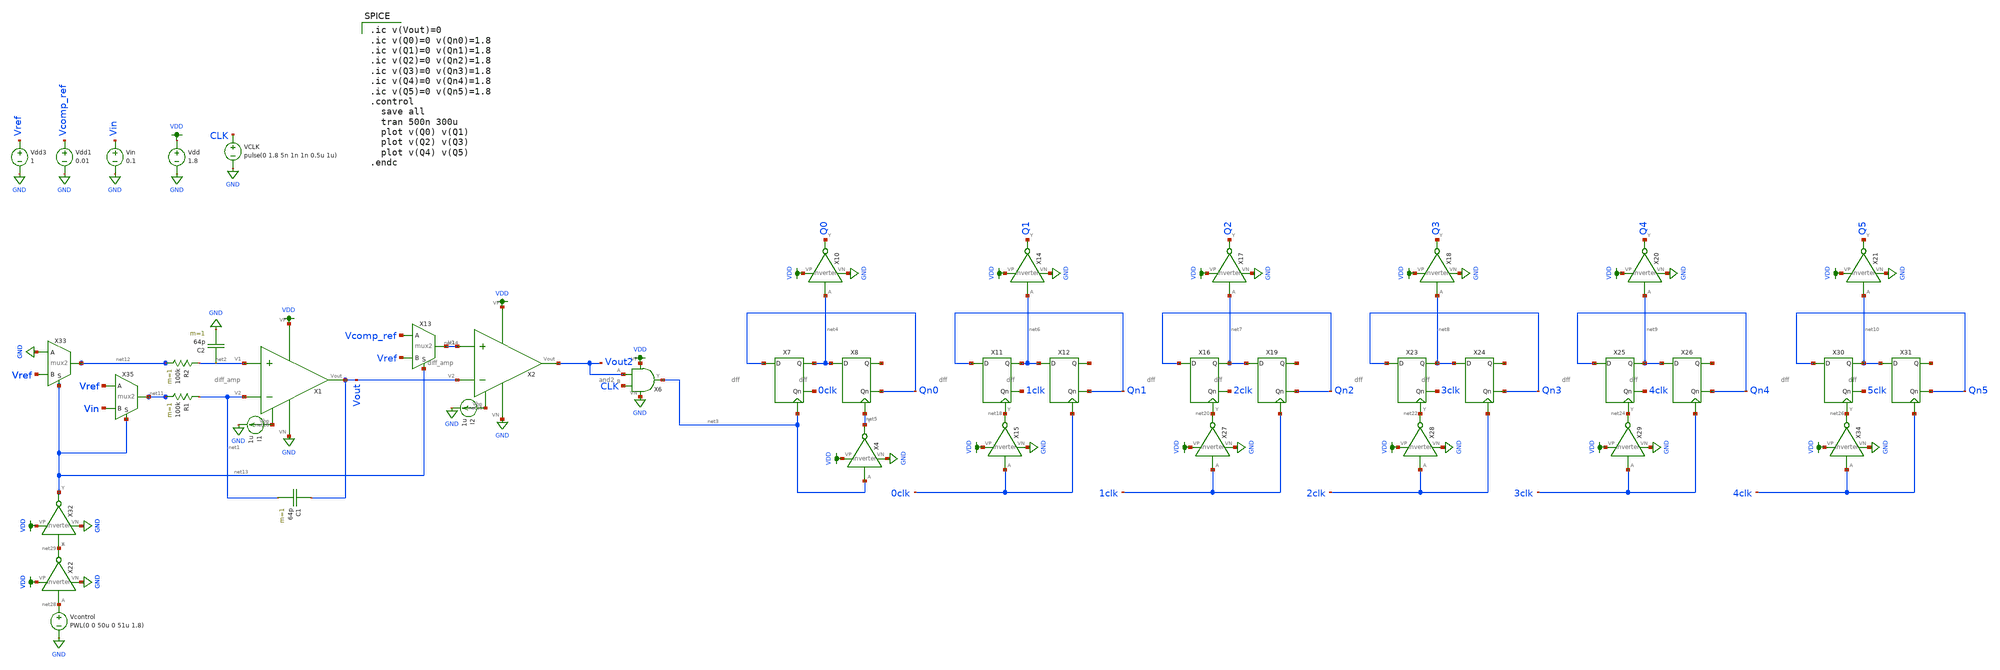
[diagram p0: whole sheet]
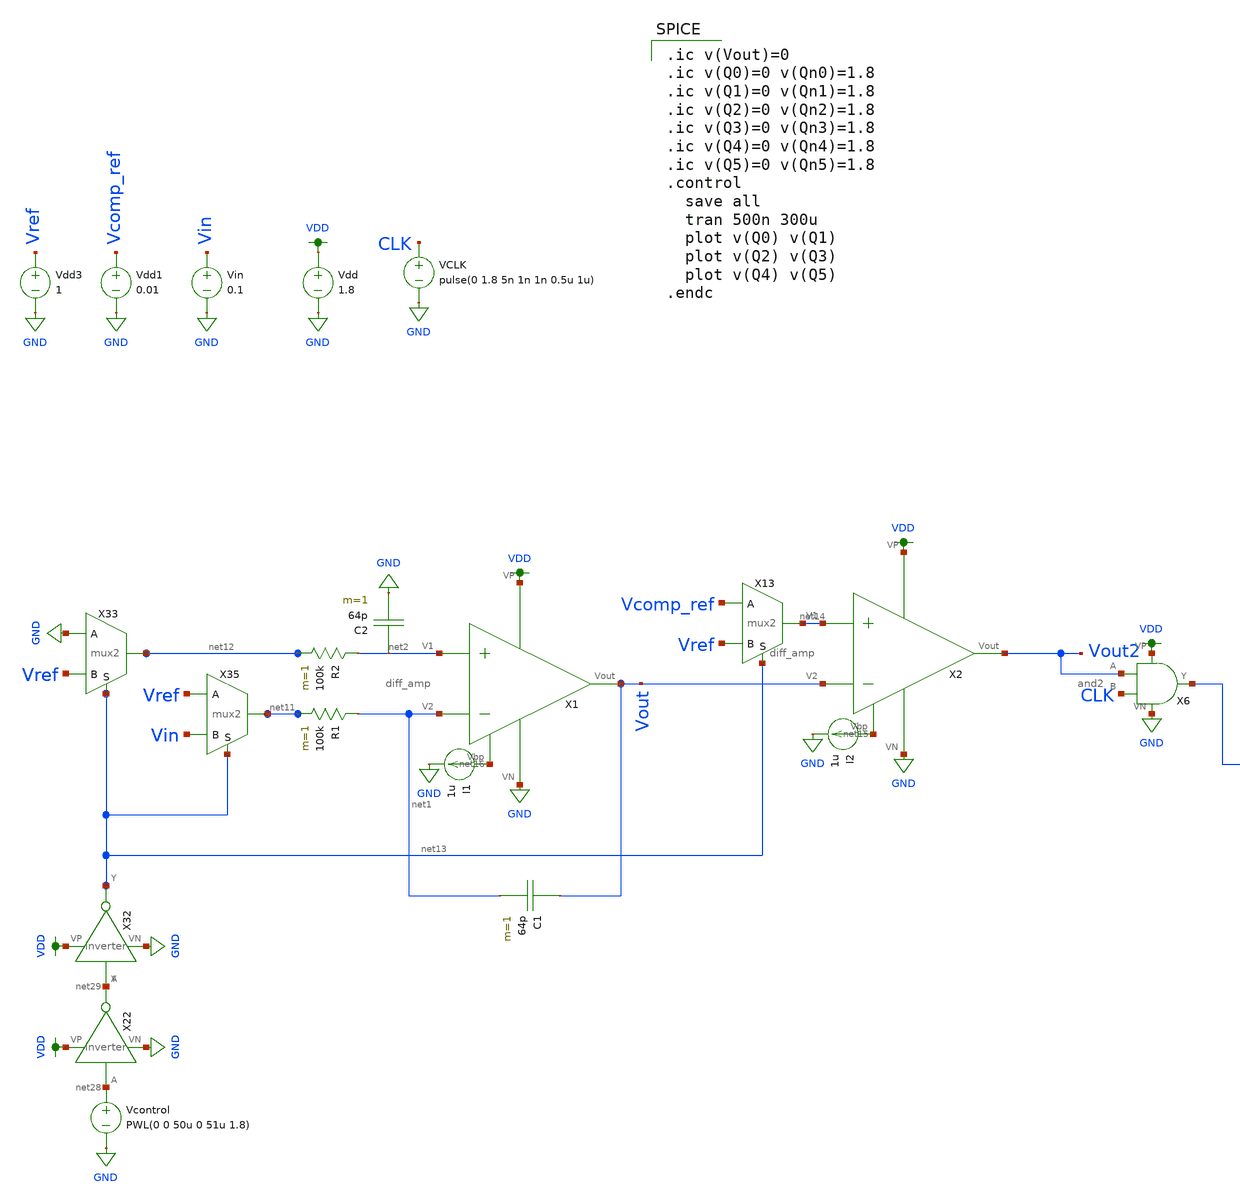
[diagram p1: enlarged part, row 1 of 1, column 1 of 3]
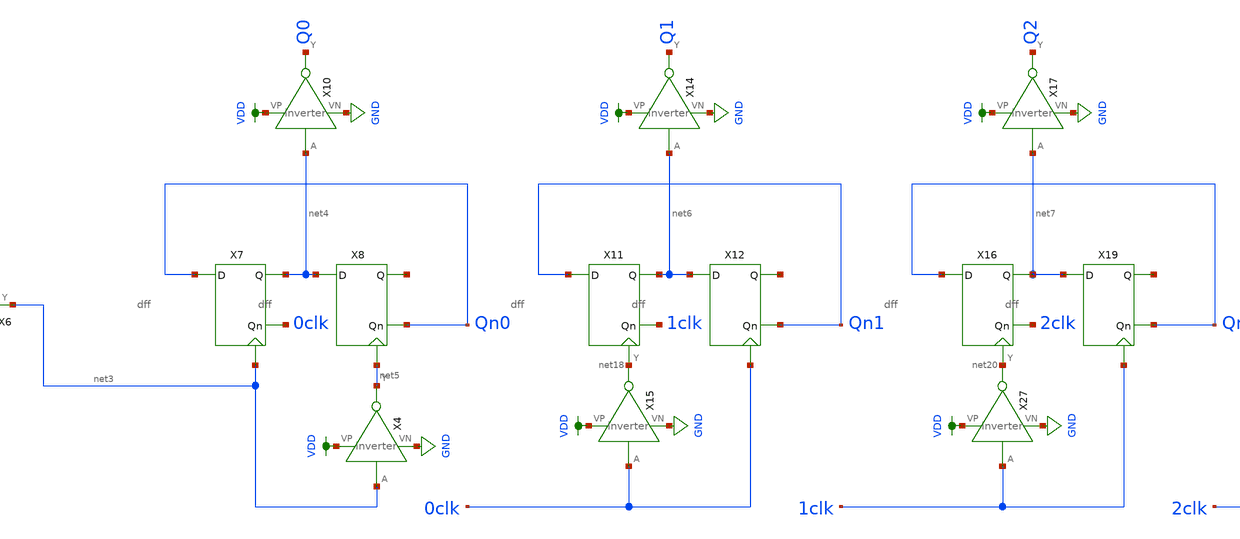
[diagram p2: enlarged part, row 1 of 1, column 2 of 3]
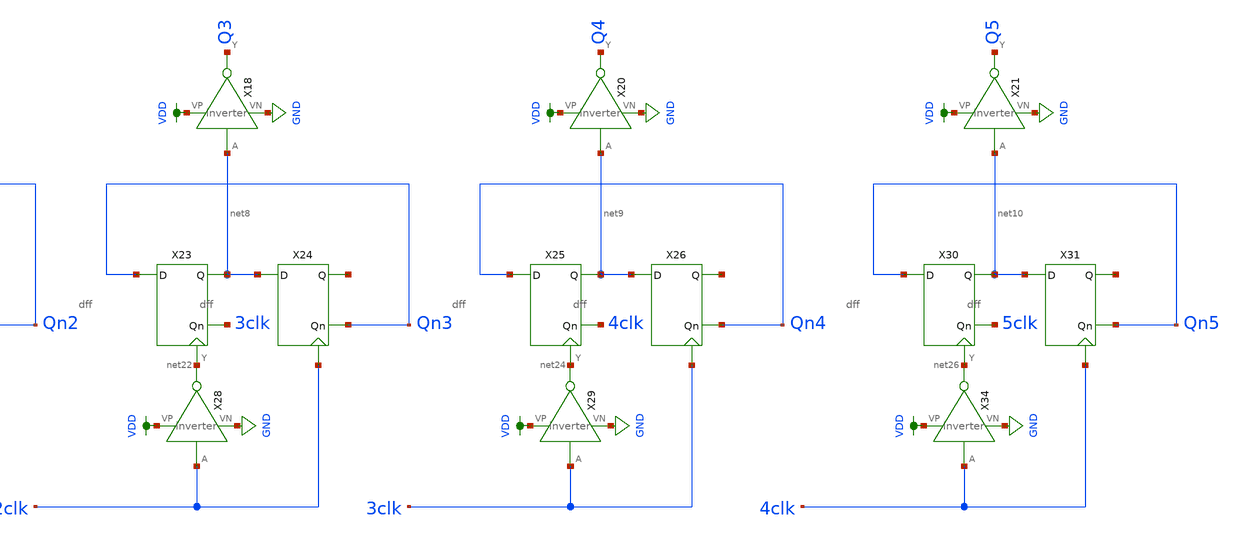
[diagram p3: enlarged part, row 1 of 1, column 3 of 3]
** sch_path: schematic/double-slope-thomas_new.sch
**.subckt double-slope-thomas_new
X2 VDD net15 Vout2 net14 Vout GND diff_amp
Vdd VDD GND 1.8
VCLK CLK GND pulse(0 1.8 5n 1n 1n 0.5u 1u)
Vdd1 Vcomp_ref GND 0.01
Vin Vin GND 0.1
I2 net15 GND 1u
C1 Vout net1 64p m=1
X1 VDD net16 Vout net2 net1 GND diff_amp
R1 net1 net11 100k m=1
C2 net2 GND 64p m=1
R2 net2 net12 100k m=1
I1 net16 GND 1u
Vdd3 Vref GND 1
X6 VDD Vout2 GND net3 CLK and2
X7 Qn0 0clk net4 net3 dff
X8 net4 Qn0 net17 net5 dff
X10 net4 Q0 VDD GND inverter
X11 Qn1 1clk net6 net18 dff
X12 net6 Qn1 net19 0clk dff
X15 0clk net18 VDD GND inverter
X16 Qn2 2clk net7 net20 dff
X19 net7 Qn2 net21 1clk dff
X23 Qn3 3clk net8 net22 dff
X24 net8 Qn3 net23 2clk dff
X25 Qn4 4clk net9 net24 dff
X26 net9 Qn4 net25 3clk dff
X27 1clk net20 VDD GND inverter
X28 2clk net22 VDD GND inverter
X29 3clk net24 VDD GND inverter
X30 Qn5 5clk net10 net26 dff
X31 net10 Qn5 net27 4clk dff
X34 4clk net26 VDD GND inverter
X13 net14 Vcomp_ref Vref net13 mux2
Vcontrol net28 GND PWL(0 0 50u 0 51u 1.8)
X14 net6 Q1 VDD GND inverter
X17 net7 Q2 VDD GND inverter
X18 net8 Q3 VDD GND inverter
X20 net9 Q4 VDD GND inverter
X21 net10 Q5 VDD GND inverter
X22 net28 net29 VDD GND inverter
X32 net29 net13 VDD GND inverter
X33 net12 GND Vref net13 mux2
X35 net11 Vref Vin net13 mux2
X4 net3 net5 VDD GND inverter
**** begin user architecture code

.ic v(Vout)=0
.ic v(Q0)=0 v(Qn0)=1.8
.ic v(Q1)=0 v(Qn1)=1.8
.ic v(Q2)=0 v(Qn2)=1.8
.ic v(Q3)=0 v(Qn3)=1.8
.ic v(Q4)=0 v(Qn4)=1.8
.ic v(Q5)=0 v(Qn5)=1.8
.control
  save all
  tran 500n 300u
  plot v(Q0) v(Q1)
  plot v(Q2) v(Q3)
  plot v(Q4) v(Q5)
.endc


.option wnflag=1
.param MC_SWITCH=0.0
.lib ~/skywater/skywater-pdk/libraries/sky130_fd_pr_ngspice/latest/models/sky130.lib.spice tt

**** end user architecture code
**.ends
.GLOBAL GND
.GLOBAL VDD
.end
